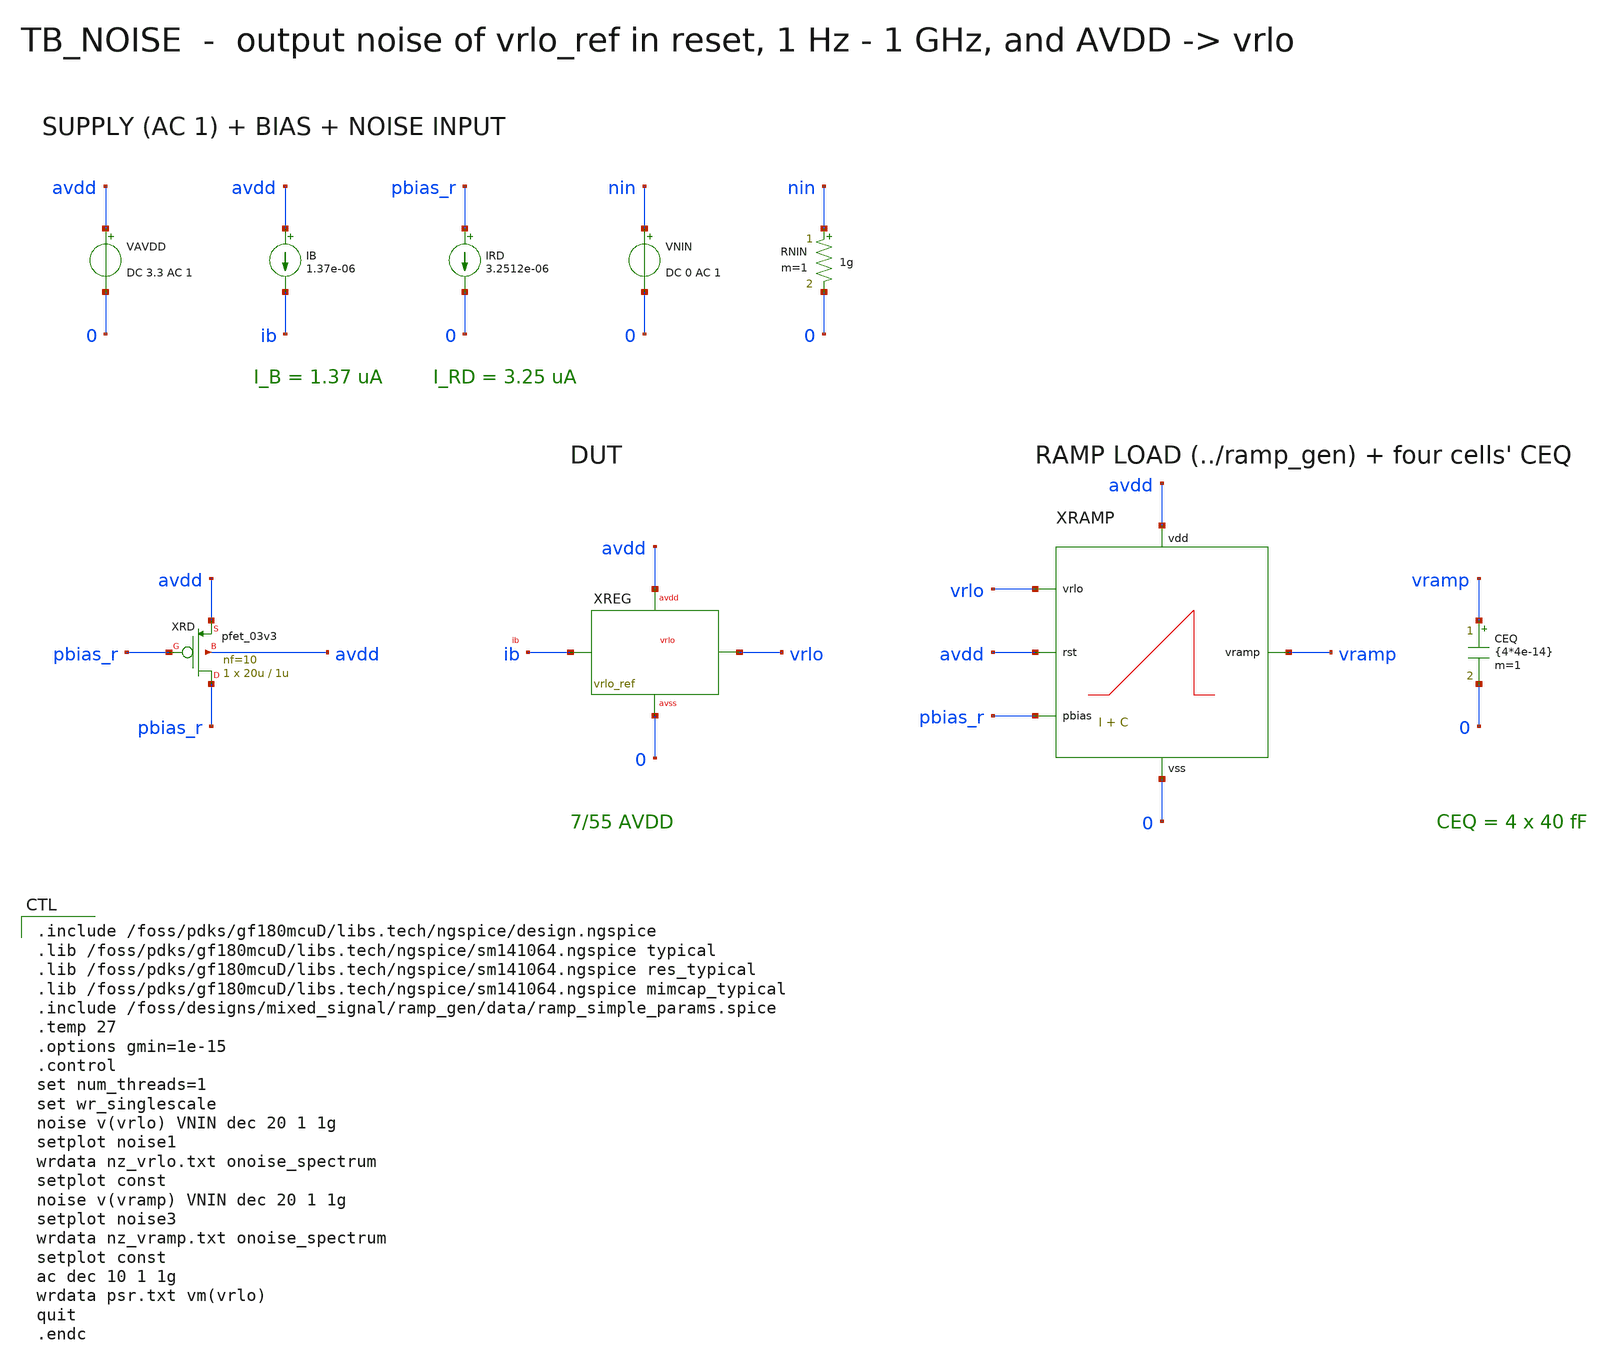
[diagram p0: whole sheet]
** sch_path: mixed_signal/vrlo_ref/tb_noise.sch
**.subckt tb_noise
VAVDD avdd 0 DC 3.3 AC 1
IB avdd ib 1.37e-06
XREG vrlo ib avdd 0 vrlo_ref
IRD pbias_r 0 3.2512e-06
XRD pbias_r pbias_r avdd avdd pfet_03v3 L=1u W=20u nf=10 m=1
XRAMP vramp avdd vrlo pbias_r avdd 0 ramp_simple
CEQ vramp 0 {4*4e-14} m=1
VNIN nin 0 DC 0 AC 1
RNIN nin 0 1g m=1
**** begin user architecture code

.include /foss/pdks/gf180mcuD/libs.tech/ngspice/design.ngspice
.lib /foss/pdks/gf180mcuD/libs.tech/ngspice/sm141064.ngspice typical
.lib /foss/pdks/gf180mcuD/libs.tech/ngspice/sm141064.ngspice res_typical
.lib /foss/pdks/gf180mcuD/libs.tech/ngspice/sm141064.ngspice mimcap_typical
.include /foss/designs/mixed_signal/ramp_gen/data/ramp_simple_params.spice
.temp 27
.options gmin=1e-15
.control
set num_threads=1
set wr_singlescale
noise v(vrlo) VNIN dec 20 1 1g
setplot noise1
wrdata nz_vrlo.txt onoise_spectrum
setplot const
noise v(vramp) VNIN dec 20 1 1g
setplot noise3
wrdata nz_vramp.txt onoise_spectrum
setplot const
ac dec 10 1 1g
wrdata psr.txt vm(vrlo)
quit
.endc

**** end user architecture code
**.ends
.end
